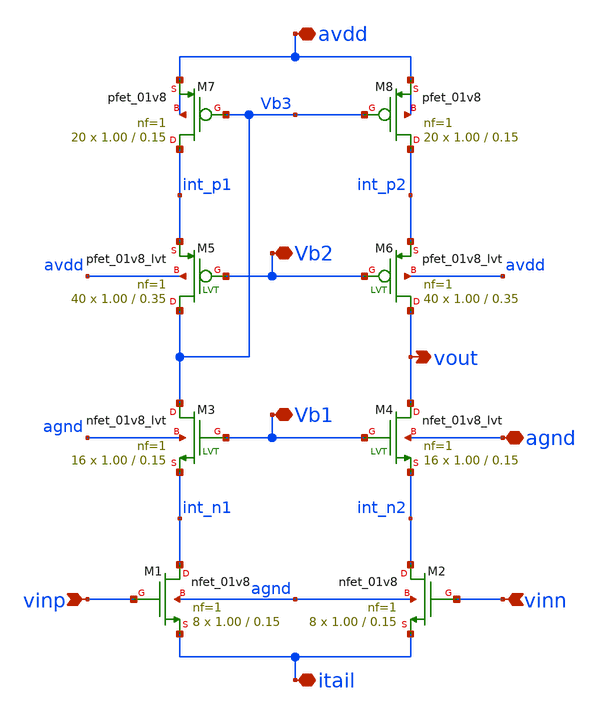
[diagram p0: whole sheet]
** sch_path: AMP/Hard_Cascode.sch
**.subckt Hard_Cascode avdd vinp vout agnd vinn Vb2 Vb1 itail
*.iopin avdd
*.ipin vinp
*.opin vout
*.iopin agnd
*.ipin vinn
*.iopin Vb2
*.iopin Vb1
*.iopin itail
XM1 int_n1 vinp itail agnd sky130_fd_pr__nfet_01v8 L=0.15 W=1.00 nf=1 ad='int((nf+1)/2) * W/nf * 0.29'
+ as='int((nf+2)/2) * W/nf * 0.29' pd='2*int((nf+1)/2) * (W/nf + 0.29)' ps='2*int((nf+2)/2) * (W/nf + 0.29)'
+ nrd='0.29 / W' nrs='0.29 / W' sa=0 sb=0 sd=0 mult=8 m=8
XM2 int_n2 vinn itail agnd sky130_fd_pr__nfet_01v8 L=0.15 W=1.00 nf=1 ad='int((nf+1)/2) * W/nf * 0.29'
+ as='int((nf+2)/2) * W/nf * 0.29' pd='2*int((nf+1)/2) * (W/nf + 0.29)' ps='2*int((nf+2)/2) * (W/nf + 0.29)'
+ nrd='0.29 / W' nrs='0.29 / W' sa=0 sb=0 sd=0 mult=8 m=8
XM7 int_p1 Vb3 avdd avdd sky130_fd_pr__pfet_01v8 L=0.15 W=1.00 nf=1 ad='int((nf+1)/2) * W/nf * 0.29'
+ as='int((nf+2)/2) * W/nf * 0.29' pd='2*int((nf+1)/2) * (W/nf + 0.29)' ps='2*int((nf+2)/2) * (W/nf + 0.29)'
+ nrd='0.29 / W' nrs='0.29 / W' sa=0 sb=0 sd=0 mult=20 m=20
XM8 int_p2 Vb3 avdd avdd sky130_fd_pr__pfet_01v8 L=0.15 W=1.00 nf=1 ad='int((nf+1)/2) * W/nf * 0.29'
+ as='int((nf+2)/2) * W/nf * 0.29' pd='2*int((nf+1)/2) * (W/nf + 0.29)' ps='2*int((nf+2)/2) * (W/nf + 0.29)'
+ nrd='0.29 / W' nrs='0.29 / W' sa=0 sb=0 sd=0 mult=20 m=20
XM3 Vb3 Vb1 int_n1 agnd sky130_fd_pr__nfet_01v8_lvt L=0.15 W=1.00 nf=1 ad='int((nf+1)/2) * W/nf * 0.29'
+ as='int((nf+2)/2) * W/nf * 0.29' pd='2*int((nf+1)/2) * (W/nf + 0.29)' ps='2*int((nf+2)/2) * (W/nf + 0.29)'
+ nrd='0.29 / W' nrs='0.29 / W' sa=0 sb=0 sd=0 mult=16 m=16
XM4 vout Vb1 int_n2 agnd sky130_fd_pr__nfet_01v8_lvt L=0.15 W=1.00 nf=1 ad='int((nf+1)/2) * W/nf * 0.29'
+ as='int((nf+2)/2) * W/nf * 0.29' pd='2*int((nf+1)/2) * (W/nf + 0.29)' ps='2*int((nf+2)/2) * (W/nf + 0.29)'
+ nrd='0.29 / W' nrs='0.29 / W' sa=0 sb=0 sd=0 mult=16 m=16
XM5 Vb3 Vb2 int_p1 avdd sky130_fd_pr__pfet_01v8_lvt L=0.35 W=1.00 nf=1 ad='int((nf+1)/2) * W/nf * 0.29'
+ as='int((nf+2)/2) * W/nf * 0.29' pd='2*int((nf+1)/2) * (W/nf + 0.29)' ps='2*int((nf+2)/2) * (W/nf + 0.29)'
+ nrd='0.29 / W' nrs='0.29 / W' sa=0 sb=0 sd=0 mult=40 m=40
XM6 vout Vb2 int_p2 avdd sky130_fd_pr__pfet_01v8_lvt L=0.35 W=1.00 nf=1 ad='int((nf+1)/2) * W/nf * 0.29'
+ as='int((nf+2)/2) * W/nf * 0.29' pd='2*int((nf+1)/2) * (W/nf + 0.29)' ps='2*int((nf+2)/2) * (W/nf + 0.29)'
+ nrd='0.29 / W' nrs='0.29 / W' sa=0 sb=0 sd=0 mult=40 m=40
**** begin user architecture code
type=primative
**** end user architecture code
**.ends
.end
